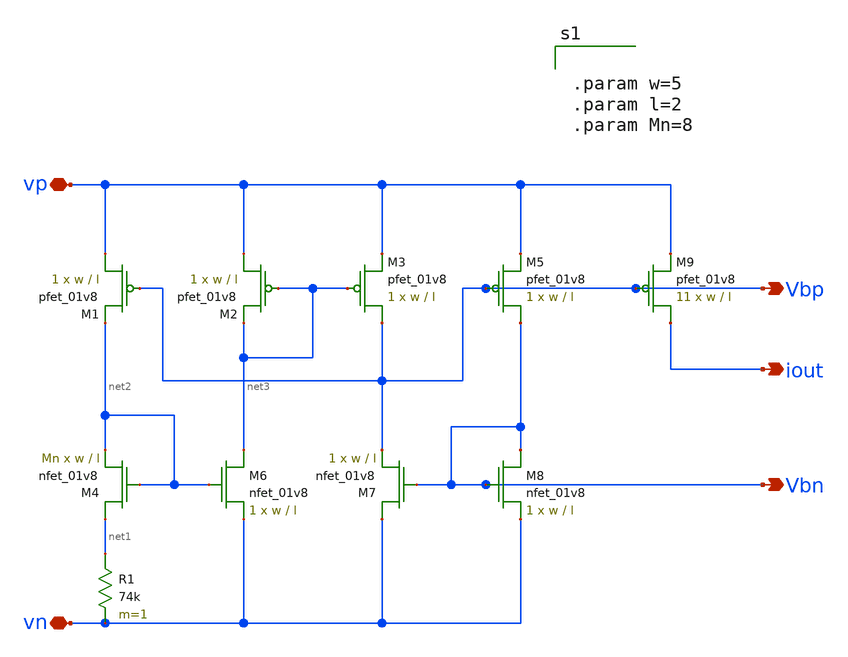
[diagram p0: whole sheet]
** sch_path: schematic/bias_current_resistive.sch
**.subckt bias_current_resistive vp vn iout Vbp Vbn
*.iopin vp
*.iopin vn
*.opin iout
*.opin Vbp
*.opin Vbn
XM1 vp Vbp net2 VDD sky130_fd_pr__pfet_01v8 L=l W=w nf=1 ad='int((nf+1)/2) * W/nf * 0.29' as='int((nf+2)/2) * W/nf * 0.29'
+ pd='2*int((nf+1)/2) * (W/nf + 0.29)' ps='2*int((nf+2)/2) * (W/nf + 0.29)' nrd='0.29 / W' nrs='0.29 / W'
+ sa=0 sb=0 sd=0 mult=1 m=1
XM2 vp net3 net3 VDD sky130_fd_pr__pfet_01v8 L=l W=w nf=1 ad='int((nf+1)/2) * W/nf * 0.29' as='int((nf+2)/2) * W/nf * 0.29'
+ pd='2*int((nf+1)/2) * (W/nf + 0.29)' ps='2*int((nf+2)/2) * (W/nf + 0.29)' nrd='0.29 / W' nrs='0.29 / W'
+ sa=0 sb=0 sd=0 mult=1 m=1
XM3 Vbp net3 vp VDD sky130_fd_pr__pfet_01v8 L=l W=w nf=1 ad='int((nf+1)/2) * W/nf * 0.29' as='int((nf+2)/2) * W/nf * 0.29'
+ pd='2*int((nf+1)/2) * (W/nf + 0.29)' ps='2*int((nf+2)/2) * (W/nf + 0.29)' nrd='0.29 / W' nrs='0.29 / W'
+ sa=0 sb=0 sd=0 mult=1 m=1
XM5 Vbn Vbp vp VDD sky130_fd_pr__pfet_01v8 L=l W=w nf=1 ad='int((nf+1)/2) * W/nf * 0.29' as='int((nf+2)/2) * W/nf * 0.29'
+ pd='2*int((nf+1)/2) * (W/nf + 0.29)' ps='2*int((nf+2)/2) * (W/nf + 0.29)' nrd='0.29 / W' nrs='0.29 / W'
+ sa=0 sb=0 sd=0 mult=1 m=1
XM4 net1 net2 net2 GND sky130_fd_pr__nfet_01v8 L=l W=w nf=1 ad='int((nf+1)/2) * W/nf * 0.29' as='int((nf+2)/2) * W/nf * 0.29'
+ pd='2*int((nf+1)/2) * (W/nf + 0.29)' ps='2*int((nf+2)/2) * (W/nf + 0.29)' nrd='0.29 / W' nrs='0.29 / W'
+ sa=0 sb=0 sd=0 mult=Mn m=Mn
XM6 net3 net2 vn GND sky130_fd_pr__nfet_01v8 L=l W=w nf=1 ad='int((nf+1)/2) * W/nf * 0.29' as='int((nf+2)/2) * W/nf * 0.29'
+ pd='2*int((nf+1)/2) * (W/nf + 0.29)' ps='2*int((nf+2)/2) * (W/nf + 0.29)' nrd='0.29 / W' nrs='0.29 / W'
+ sa=0 sb=0 sd=0 mult=1 m=1
XM7 vn Vbn Vbp GND sky130_fd_pr__nfet_01v8 L=l W=w nf=1 ad='int((nf+1)/2) * W/nf * 0.29' as='int((nf+2)/2) * W/nf * 0.29'
+ pd='2*int((nf+1)/2) * (W/nf + 0.29)' ps='2*int((nf+2)/2) * (W/nf + 0.29)' nrd='0.29 / W' nrs='0.29 / W'
+ sa=0 sb=0 sd=0 mult=1 m=1
XM8 Vbn Vbn vn GND sky130_fd_pr__nfet_01v8 L=l W=w nf=1 ad='int((nf+1)/2) * W/nf * 0.29' as='int((nf+2)/2) * W/nf * 0.29'
+ pd='2*int((nf+1)/2) * (W/nf + 0.29)' ps='2*int((nf+2)/2) * (W/nf + 0.29)' nrd='0.29 / W' nrs='0.29 / W'
+ sa=0 sb=0 sd=0 mult=1 m=1
R1 net1 vn 74k m=1
XM9 iout Vbp vp VDD sky130_fd_pr__pfet_01v8 L=l W=w nf=1 ad='int((nf+1)/2) * W/nf * 0.29' as='int((nf+2)/2) * W/nf * 0.29'
+ pd='2*int((nf+1)/2) * (W/nf + 0.29)' ps='2*int((nf+2)/2) * (W/nf + 0.29)' nrd='0.29 / W' nrs='0.29 / W'
+ sa=0 sb=0 sd=0 mult=11 m=11
**** begin user architecture code


.param w=5
.param l=2
.param Mn=8


**** end user architecture code
**.ends
.end
